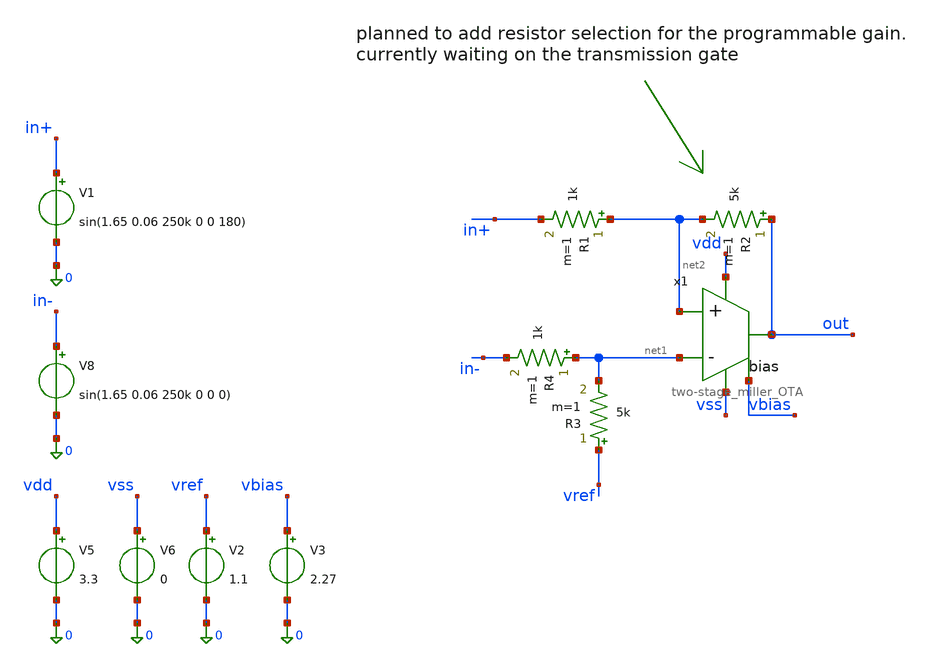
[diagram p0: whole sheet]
** sch_path: design/analog/PGA + differential to single ended converter/PGA + diff_converter.sch
**.subckt PGA + diff_converter
V5 vdd 0 3.3
V6 vss 0 0
V8 in- 0 sin(1.65 0.06 250k 0 0 0)
V1 in+ 0 sin(1.65 0.06 250k 0 0 180)
x1 vdd out net2 net1 vbias vss two-stage_miller_OTA
R1 net2 in+ 1k m=1
V2 vref 0 1.1
R3 vref net1 5k m=1
R4 net1 in- 1k m=1
R2 out net2 5k m=1
V3 vbias 0 2.27
**.ends

* expanding   symbol:  acoustic_ranger_2026/two-stage_miller_OTA.sym # of pins=6
** sym_path: design/analog/OTA/two-stage_miller_OTA.sym
** sch_path: design/analog/OTA/two-stage_miller_OTA.sch
.subckt two-stage_miller_OTA vdd out in+ in- bias vss
*.ipin in+
*.ipin in-
*.opin out
*.iopin vdd
*.iopin vss
*.ipin bias
XM1 net2 in- net1 vdd pfet_03v3 L=1u W=6.2u nf=1 ad='int((nf+1)/2) * W/nf * 0.18u' as='int((nf+2)/2) * W/nf * 0.18u'
+ pd='2*int((nf+1)/2) * (W/nf + 0.18u)' ps='2*int((nf+2)/2) * (W/nf + 0.18u)' nrd='0.18u / W' nrs='0.18u / W'
+ sa=0 sb=0 sd=0 m=8
XM2 net3 in+ net1 vdd pfet_03v3 L=1u W=6.2u nf=1 ad='int((nf+1)/2) * W/nf * 0.18u' as='int((nf+2)/2) * W/nf * 0.18u'
+ pd='2*int((nf+1)/2) * (W/nf + 0.18u)' ps='2*int((nf+2)/2) * (W/nf + 0.18u)' nrd='0.18u / W' nrs='0.18u / W'
+ sa=0 sb=0 sd=0 m=8
XM14 net3 net2 vss vss nfet_03v3 L=3u W=7.7u nf=4 ad='int((nf+1)/2) * W/nf * 0.18u' as='int((nf+2)/2) * W/nf * 0.18u'
+ pd='2*int((nf+1)/2) * (W/nf + 0.18u)' ps='2*int((nf+2)/2) * (W/nf + 0.18u)' nrd='0.18u / W' nrs='0.18u / W'
+ sa=0 sb=0 sd=0 m=2
XM15 net2 net2 vss vss nfet_03v3 L=3u W=7.7u nf=4 ad='int((nf+1)/2) * W/nf * 0.18u' as='int((nf+2)/2) * W/nf * 0.18u'
+ pd='2*int((nf+1)/2) * (W/nf + 0.18u)' ps='2*int((nf+2)/2) * (W/nf + 0.18u)' nrd='0.18u / W' nrs='0.18u / W'
+ sa=0 sb=0 sd=0 m=2
XM3 out net3 vss vss nfet_03v3 L=3u W=7.7u nf=4 ad='int((nf+1)/2) * W/nf * 0.18u' as='int((nf+2)/2) * W/nf * 0.18u'
+ pd='2*int((nf+1)/2) * (W/nf + 0.18u)' ps='2*int((nf+2)/2) * (W/nf + 0.18u)' nrd='0.18u / W' nrs='0.18u / W'
+ sa=0 sb=0 sd=0 m=12
C1 out net3 5p m=1
XM4 net1 bias vdd vdd pfet_03v3 L=20u W=25.3u nf=2 ad='int((nf+1)/2) * W/nf * 0.18u' as='int((nf+2)/2) * W/nf * 0.18u'
+ pd='2*int((nf+1)/2) * (W/nf + 0.18u)' ps='2*int((nf+2)/2) * (W/nf + 0.18u)' nrd='0.18u / W' nrs='0.18u / W'
+ sa=0 sb=0 sd=0 m=2
XM5 out bias vdd vdd pfet_03v3 L=20u W=25.3u nf=2 ad='int((nf+1)/2) * W/nf * 0.18u' as='int((nf+2)/2) * W/nf * 0.18u'
+ pd='2*int((nf+1)/2) * (W/nf + 0.18u)' ps='2*int((nf+2)/2) * (W/nf + 0.18u)' nrd='0.18u / W' nrs='0.18u / W'
+ sa=0 sb=0 sd=0 m=6
.ends

.end
